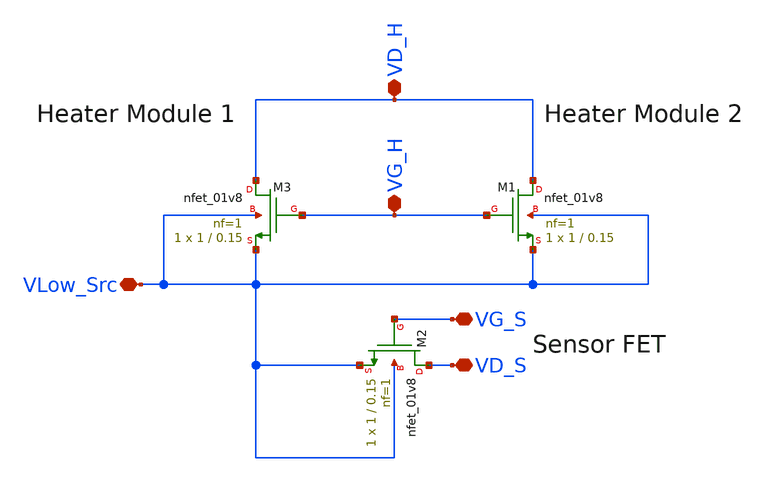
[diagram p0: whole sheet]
** sch_path: xschem/HSense_nFET_1f1WL150n_V6.sch
**.subckt HSense_nFET_1f1WL150n_V6 VG_H VD_H VG_S VD_S VLow_Src
*.iopin VG_H
*.iopin VD_H
*.iopin VG_S
*.iopin VD_S
*.iopin VLow_Src
XM1 VD_H VG_H VLow_Src VLow_Src sky130_fd_pr__nfet_01v8 L=0.15 W=1 nf=1 ad='int((nf+1)/2) * W/nf * 0.29'
+ as='int((nf+2)/2) * W/nf * 0.29' pd='2*int((nf+1)/2) * (W/nf + 0.29)' ps='2*int((nf+2)/2) * (W/nf + 0.29)'
+ nrd='0.29 / W' nrs='0.29 / W' sa=0 sb=0 sd=0 mult=1 m=1
XM2 VD_S VG_S VLow_Src VLow_Src sky130_fd_pr__nfet_01v8 L=0.15 W=1 nf=1 ad='int((nf+1)/2) * W/nf * 0.29'
+ as='int((nf+2)/2) * W/nf * 0.29' pd='2*int((nf+1)/2) * (W/nf + 0.29)' ps='2*int((nf+2)/2) * (W/nf + 0.29)'
+ nrd='0.29 / W' nrs='0.29 / W' sa=0 sb=0 sd=0 mult=1 m=1
XM3 VD_H VG_H VLow_Src VLow_Src sky130_fd_pr__nfet_01v8 L=0.15 W=1 nf=1 ad='int((nf+1)/2) * W/nf * 0.29'
+ as='int((nf+2)/2) * W/nf * 0.29' pd='2*int((nf+1)/2) * (W/nf + 0.29)' ps='2*int((nf+2)/2) * (W/nf + 0.29)'
+ nrd='0.29 / W' nrs='0.29 / W' sa=0 sb=0 sd=0 mult=1 m=1
**.ends
.end
